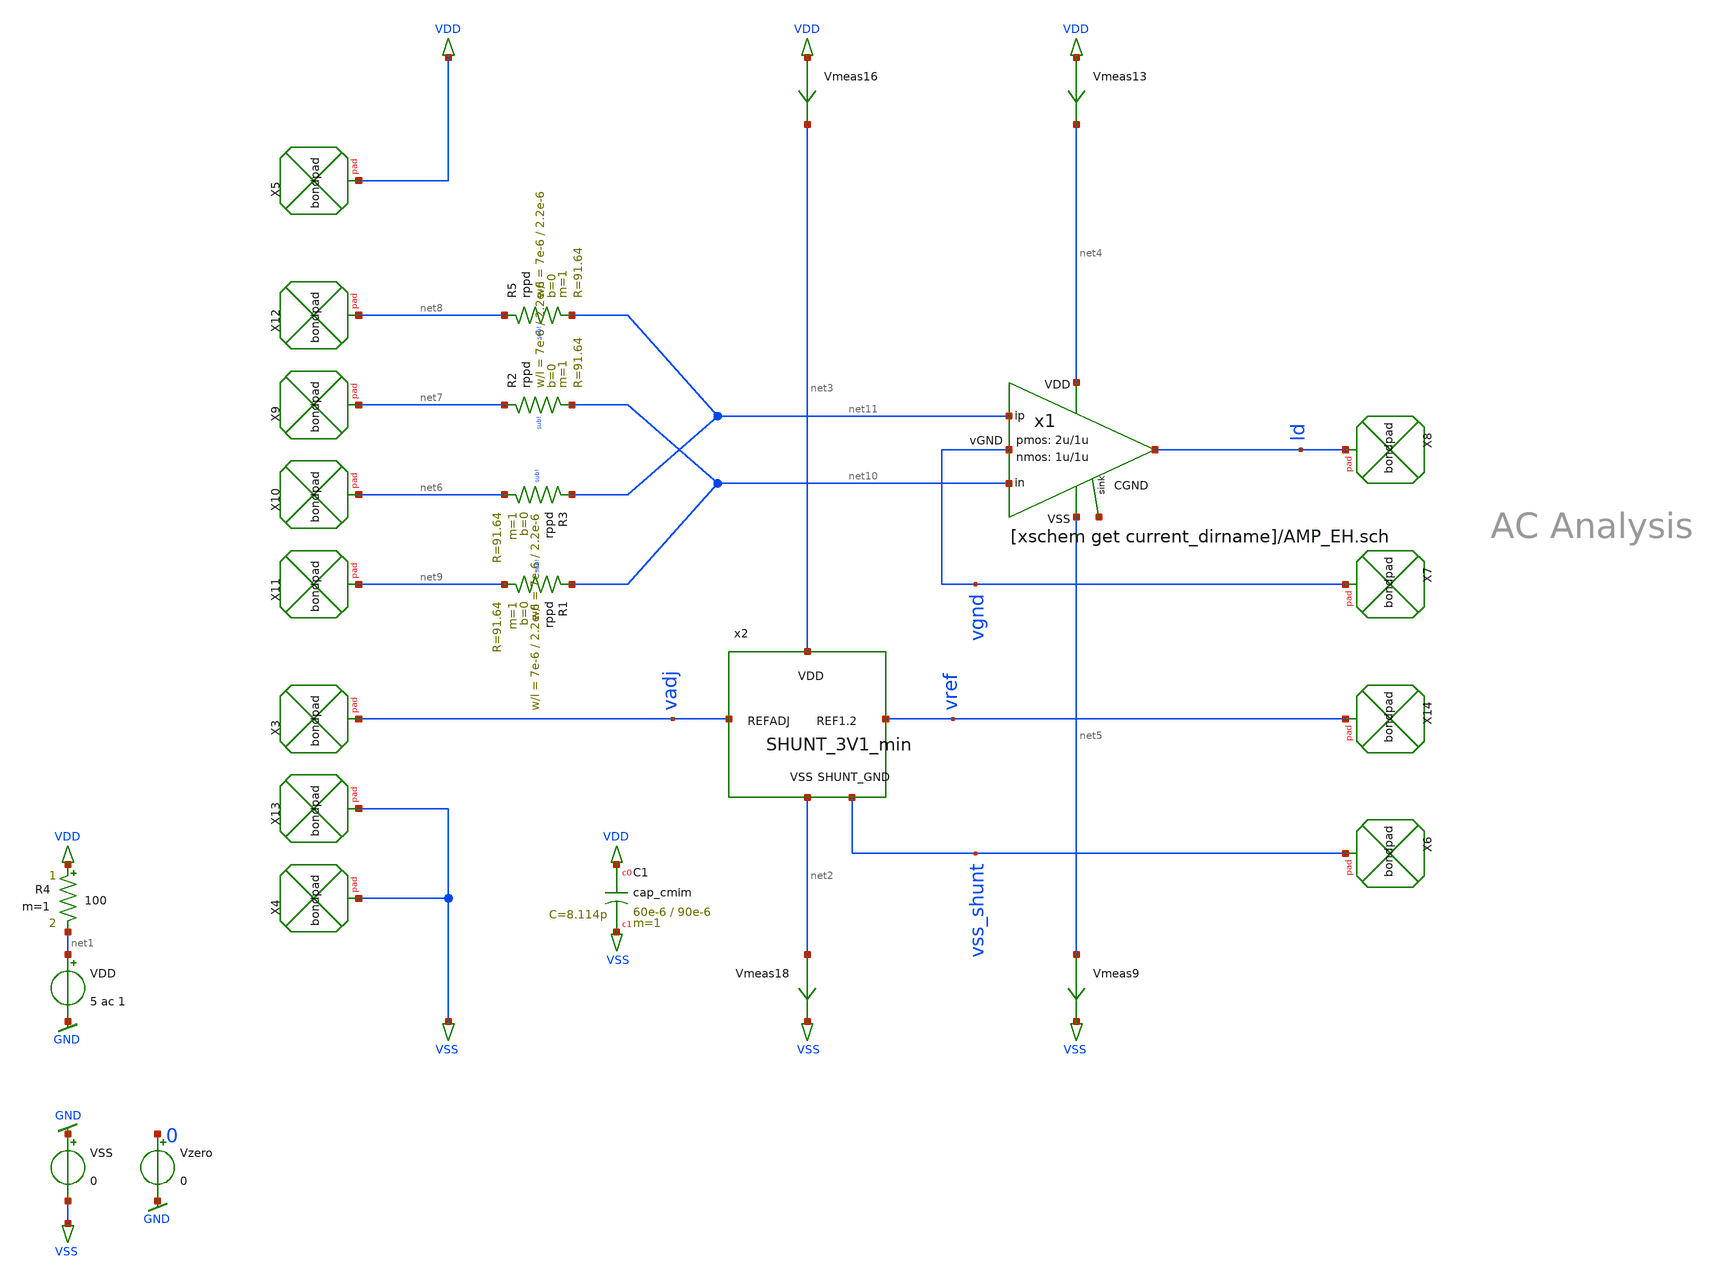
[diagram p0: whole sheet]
** sch_path: HBT_AMP_low_power/design_data/xschem/chip/FMD_QNC_HBT_AMP_EH.01.sch
* Copyright (C) 1998-2023 Stefan Frederik Schippers
* This program is free software; you can redistribute it and/or modify
* it under the terms of the GNU General Public License as published by
* the Free Software Foundation; either version 2 of the License, or
* (at your option) any later version.
* This program is distributed in the hope that it will be useful,
* but WITHOUT ANY WARRANTY; without even the implied warranty of
* MERCHANTABILITY or FITNESS FOR A PARTICULAR PURPOSE.  See the
* GNU General Public License for more details.
* You should have received a copy of the GNU General Public License
* along with this program; if not, write to the Free Software
**.subckt FMD_QNC_HBT_AMP_EH.01
VDD net1 GND 5 ac 1
VSS GND VSS 0
Vzero 0 GND 0
Vmeas13 VDD net4 0
.save i(vmeas13)
Vmeas16 VDD net3 0
.save i(vmeas16)
Vmeas18 net2 VSS 0
.save i(vmeas18)
Vmeas9 net5 VSS 0
.save i(vmeas9)
R4 VDD net1 100 m=1
x1 net4 net11 net10 net5 ld net12 vgnd AMP_EH nw=1u nl=1u pw=2u pl=1u
x2 net3 vref vadj vss_shunt net2 SHUNT_3V1_min
XX3 vadj bondpad size=80u shape=0 padtype=0
XX4 VSS bondpad size=80u shape=0 padtype=0
XX5 VDD bondpad size=80u shape=0 padtype=0
XX6 vss_shunt bondpad size=80u shape=0 padtype=0
XX7 vgnd bondpad size=80u shape=0 padtype=0
XX8 ld bondpad size=80u shape=0 padtype=0
XX9 net7 bondpad size=80u shape=0 padtype=0
XX10 net6 bondpad size=80u shape=0 padtype=0
XX11 net9 bondpad size=80u shape=0 padtype=0
XX12 net8 bondpad size=80u shape=0 padtype=0
XR3 net11 net6 sub! rppd w=7e-6 l=2.2e-6 m=1 b=0 mm_ok=1
XR1 net10 net9 sub! rppd w=7e-6 l=2.2e-6 m=1 b=0 mm_ok=1
XR2 net7 net10 sub! rppd w=7e-6 l=2.2e-6 m=1 b=0 mm_ok=1
XR5 net8 net11 sub! rppd w=7e-6 l=2.2e-6 m=1 b=0 mm_ok=1
XX14 vref bondpad size=80u shape=0 padtype=0
XX13 VSS bondpad size=80u shape=0 padtype=0
XC1 VDD VSS cap_cmim w=60e-6 l=90e-6 m=1 mm_ok=1
**** begin user architecture code









**** end user architecture code
**.ends
.GLOBAL GND
.end
